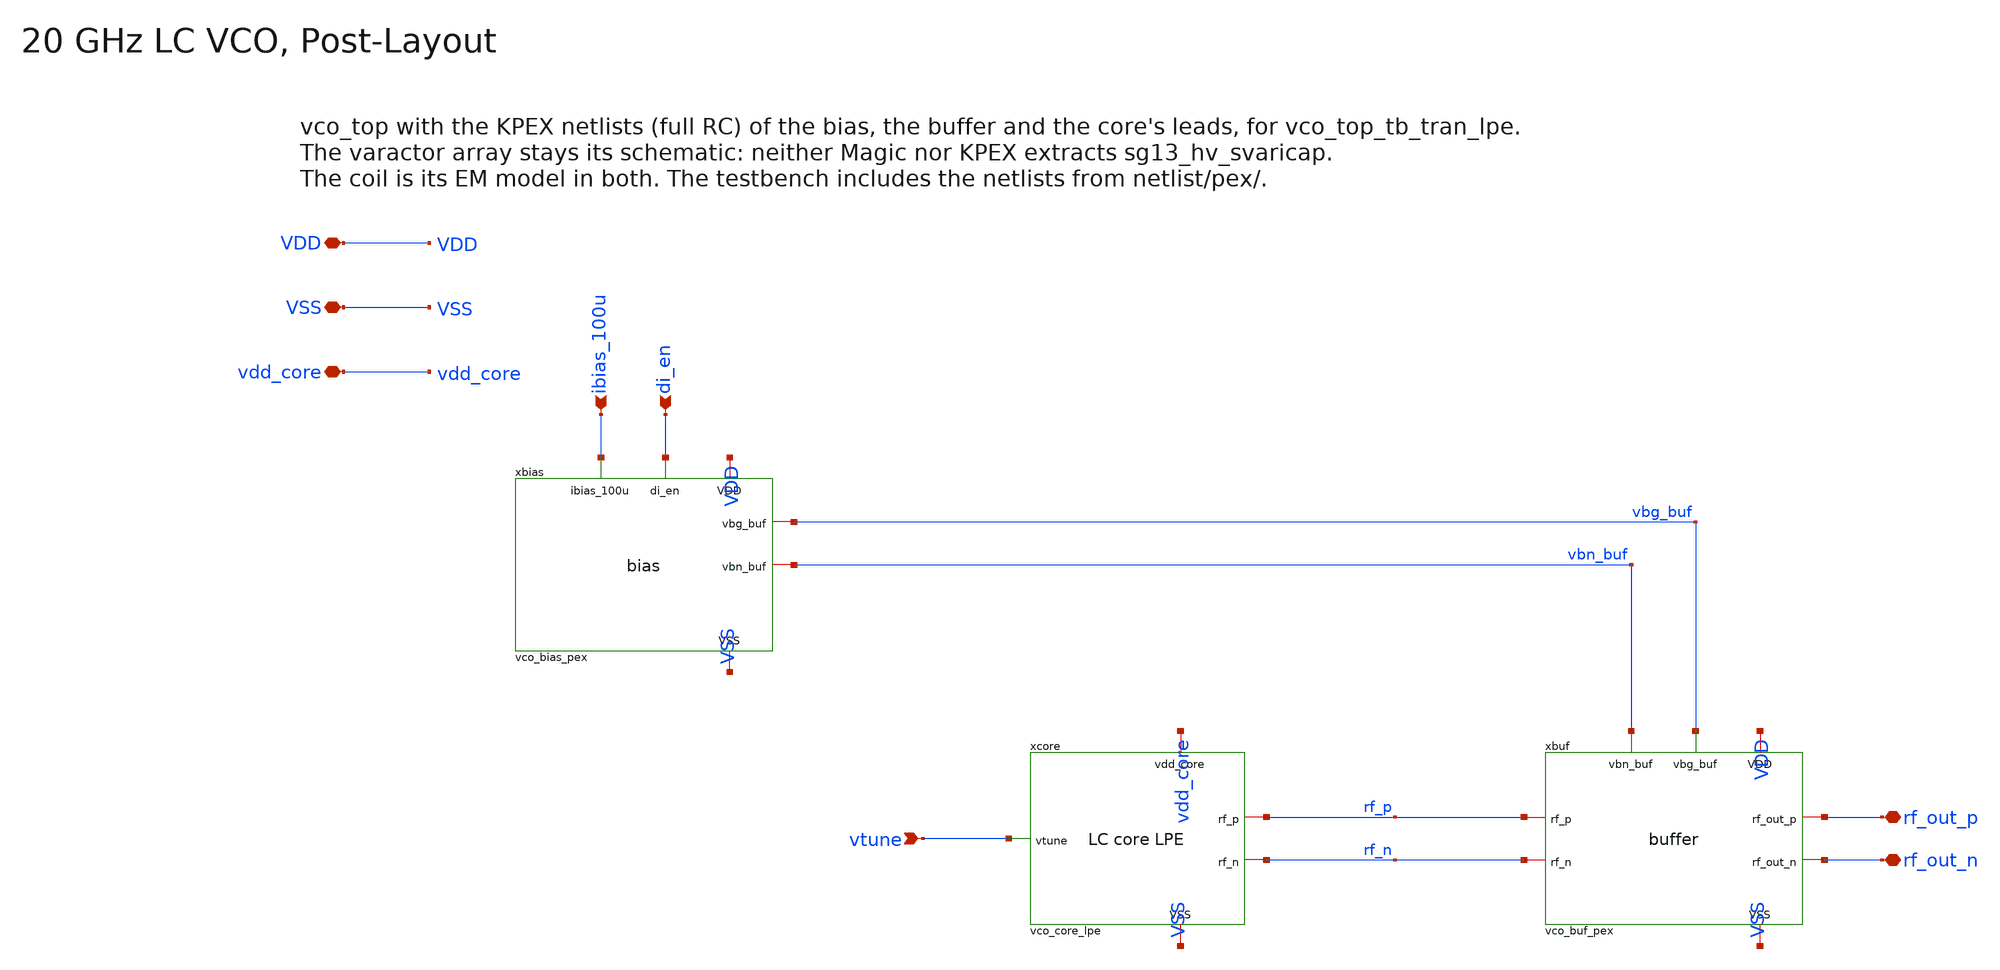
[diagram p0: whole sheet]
** sch_path: macros/vco/testbenches/xschem/vco_top_lpe.sch
**.subckt vco_top_lpe VDD VSS vdd_core ibias_100u di_en vtune rf_out_p rf_out_n
*.iopin VDD
*.iopin VSS
*.iopin vdd_core
*.ipin ibias_100u
*.ipin di_en
*.ipin vtune
*.iopin rf_out_p
*.iopin rf_out_n
xbias ibias_100u di_en VDD VSS vbg_buf vbn_buf vco_bias_pex
xcore vdd_core VSS vtune rf_p rf_n vco_core_lpe
xbuf vbn_buf vbg_buf VDD VSS rf_p rf_n rf_out_p rf_out_n vco_buf_pex
**.ends

* expanding   symbol:  vco_core_lpe.sym # of pins=5
** sym_path: macros/vco/testbenches/xschem/vco_core_lpe.sym
** sch_path: macros/vco/testbenches/xschem/vco_core_lpe.sch
.subckt vco_core_lpe vdd_core VSS vtune rf_p rf_n
*.iopin vdd_core
*.iopin VSS
*.ipin vtune
*.iopin rf_p
*.iopin rf_n
xleads vdd_core VSS vtune rf_p rf_n vco_core_leads
xind rf_p rf_n vdd_core VSS vco_ind
xvar rf_p rf_n vtune VSS vco_var
.ends


* expanding   symbol:  vco_ind.sym # of pins=4
** sym_path: macros/vco/schematic/xschem/vco_ind.sym
** sch_path: macros/vco/schematic/xschem/vco_ind.sch
.subckt vco_ind la lb lc VSS
*.iopin la
*.iopin lc
*.iopin lb
*.iopin VSS
XL1 la lc lb VSS inductor3 w=4e-6 s=4e-6 d=52e-6 nr_r=2 m=1
x1 la lb lc vco_ind_le
.ends


* expanding   symbol:  vco_var.sym # of pins=4
** sym_path: macros/vco/schematic/xschem/vco_var.sym
** sch_path: macros/vco/schematic/xschem/vco_var.sch
.subckt vco_var rf_p rf_n vtune VSS
*.ipin vtune
*.iopin rf_p
*.iopin rf_n
*.iopin VSS
XCvar1 rf_p vtune rf_n VSS sg13_hv_svaricap w=3.74u l=0.3u Nx=7 mm_ok=1
XCvar2 rf_p vtune rf_n VSS sg13_hv_svaricap w=3.74u l=0.3u Nx=7 mm_ok=1
XCvar3 rf_p vtune rf_n VSS sg13_hv_svaricap w=3.74u l=0.3u Nx=7 mm_ok=1
.ends

.end
